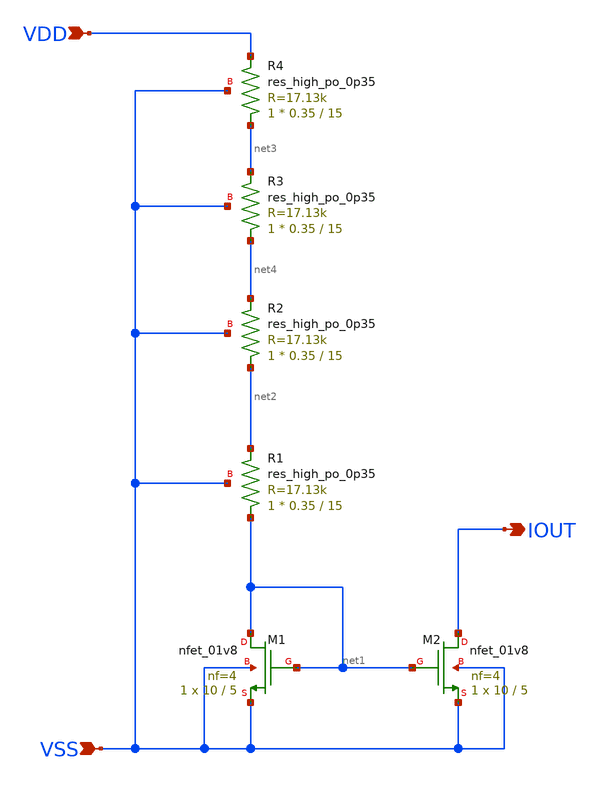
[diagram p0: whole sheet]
** sch_path: tt_um_upalermo_simple_analog_circuit/xschem/currentmirror.sch
**.subckt currentmirror IOUT VSS VDD
*.opin IOUT
*.ipin VSS
*.ipin VDD
XM1 net1 net1 VSS VSS sky130_fd_pr__nfet_01v8 L=5 W=10 nf=4 ad='int((nf+1)/2) * W/nf * 0.29' as='int((nf+2)/2) * W/nf * 0.29'
+ pd='2*int((nf+1)/2) * (W/nf + 0.29)' ps='2*int((nf+2)/2) * (W/nf + 0.29)' nrd='0.29 / W' nrs='0.29 / W'
+ sa=0 sb=0 sd=0 mult=1 m=1
XM2 IOUT net1 VSS VSS sky130_fd_pr__nfet_01v8 L=5 W=10 nf=4 ad='int((nf+1)/2) * W/nf * 0.29' as='int((nf+2)/2) * W/nf * 0.29'
+ pd='2*int((nf+1)/2) * (W/nf + 0.29)' ps='2*int((nf+2)/2) * (W/nf + 0.29)' nrd='0.29 / W' nrs='0.29 / W'
+ sa=0 sb=0 sd=0 mult=1 m=1
XR1 net1 net2 VSS sky130_fd_pr__res_high_po_0p35 L=15 mult=1 m=1
XR2 net2 net4 VSS sky130_fd_pr__res_high_po_0p35 L=15 mult=1 m=1
XR3 net4 net3 VSS sky130_fd_pr__res_high_po_0p35 L=15 mult=1 m=1
XR4 net3 VDD VSS sky130_fd_pr__res_high_po_0p35 L=15 mult=1 m=1
**.ends
.end
